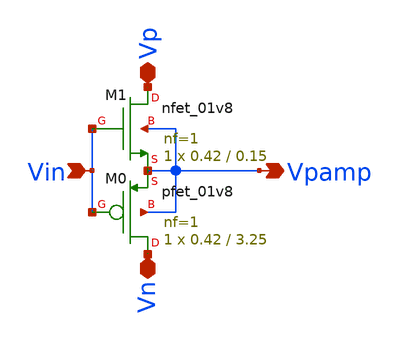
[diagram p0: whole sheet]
** sch_path: xschem/Vth_sch/Symbol/preamp.sch
**.subckt preamp Vin Vpamp Vp Vn
*.ipin Vin
*.opin Vpamp
*.iopin Vp
*.iopin Vn
XM1 Vp Vin Vpamp Vpamp sky130_fd_pr__nfet_01v8 L=0.15 W=0.42 nf=1 ad='int((nf+1)/2) * W/nf * 0.29' as='int((nf+2)/2) * W/nf * 0.29'
+ pd='2*int((nf+1)/2) * (W/nf + 0.29)' ps='2*int((nf+2)/2) * (W/nf + 0.29)' nrd='0.29 / W' nrs='0.29 / W'
+ sa=0 sb=0 sd=0 mult=1 m=1
XM0 Vn Vin Vpamp Vpamp sky130_fd_pr__pfet_01v8 L=3.25 W=0.42 nf=1 ad='int((nf+1)/2) * W/nf * 0.29' as='int((nf+2)/2) * W/nf * 0.29'
+ pd='2*int((nf+1)/2) * (W/nf + 0.29)' ps='2*int((nf+2)/2) * (W/nf + 0.29)' nrd='0.29 / W' nrs='0.29 / W'
+ sa=0 sb=0 sd=0 mult=1 m=1
**.ends
.end
